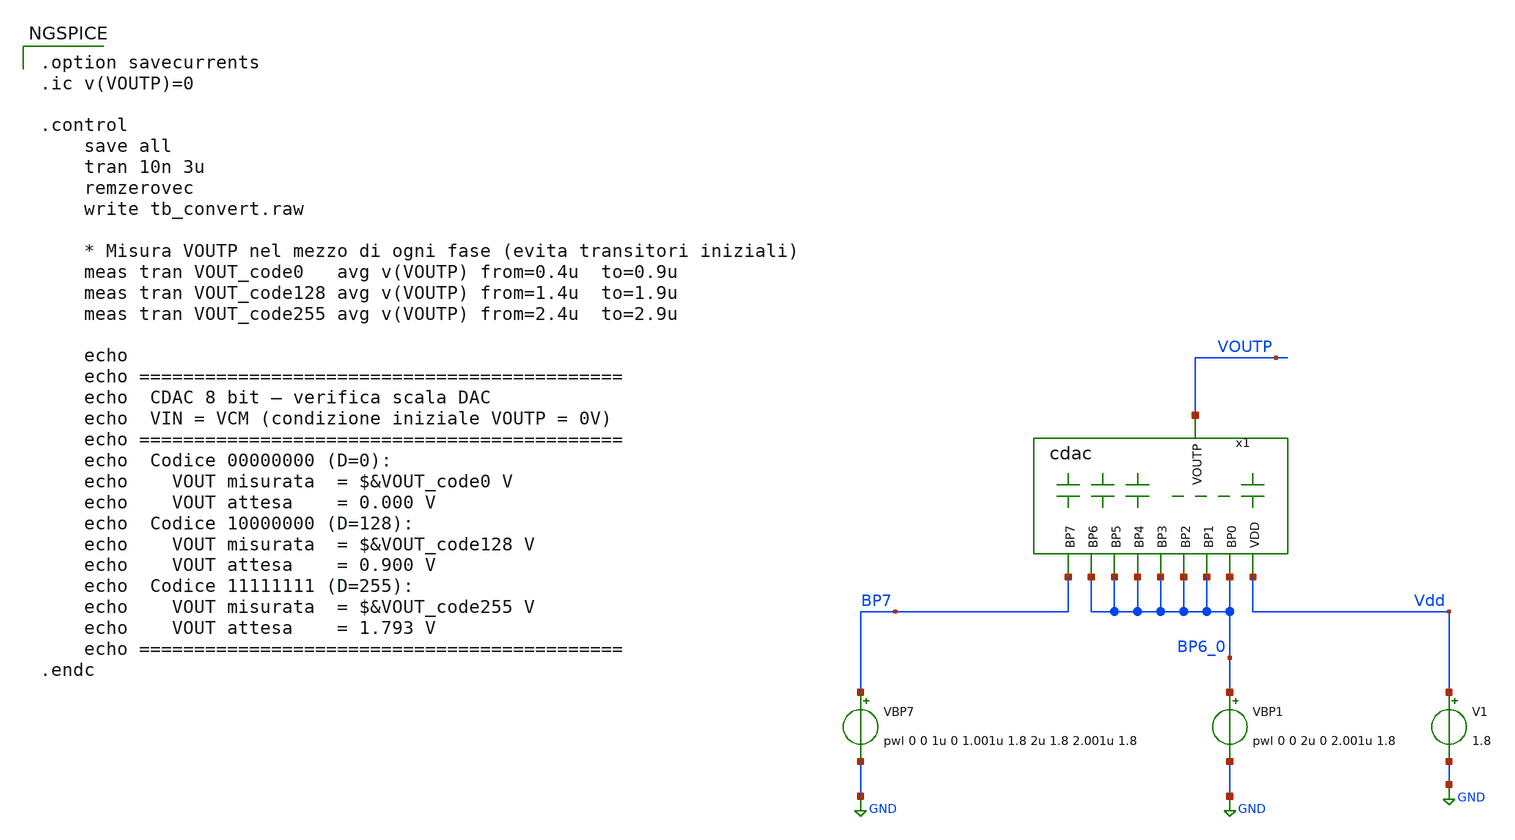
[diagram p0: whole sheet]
** sch_path: 02_sky130_pdk/soluzioni/lab_cdac/xschem/tb_convert.sch
**.subckt tb_convert
VBP7 BP7 GND pwl 0 0 1u 0 1.001u 1.8 2u 1.8 2.001u 1.8
VBP1 BP6_0 GND pwl 0 0 2u 0 2.001u 1.8
x1 VOUTP Vdd BP6_0 BP6_0 BP6_0 BP6_0 BP6_0 BP6_0 BP7 BP6_0 cdac
V1 Vdd GND 1.8
**** begin user architecture code

** opencircuitdesign pdks install
.lib $::SKYWATER_MODELS/sky130.lib.spice tt


.option savecurrents
.ic v(VOUTP)=0

.control
    save all
    tran 10n 3u
    remzerovec
    write tb_convert.raw

    * Misura VOUTP nel mezzo di ogni fase (evita transitori iniziali)
    meas tran VOUT_code0   avg v(VOUTP) from=0.4u  to=0.9u
    meas tran VOUT_code128 avg v(VOUTP) from=1.4u  to=1.9u
    meas tran VOUT_code255 avg v(VOUTP) from=2.4u  to=2.9u

    echo
    echo ============================================
    echo  CDAC 8 bit — verifica scala DAC
    echo  VIN = VCM (condizione iniziale VOUTP = 0V)
    echo ============================================
    echo  Codice 00000000 (D=0):
    echo    VOUT misurata  = $&VOUT_code0 V
    echo    VOUT attesa    = 0.000 V
    echo  Codice 10000000 (D=128):
    echo    VOUT misurata  = $&VOUT_code128 V
    echo    VOUT attesa    = 0.900 V
    echo  Codice 11111111 (D=255):
    echo    VOUT misurata  = $&VOUT_code255 V
    echo    VOUT attesa    = 1.793 V
    echo ============================================
.endc

**** end user architecture code
**.ends

* expanding   symbol:  cdac.sym # of pins=10
** sym_path: 02_sky130_pdk/soluzioni/lab_cdac/xschem/cdac.sym
** sch_path: 02_sky130_pdk/soluzioni/lab_cdac/xschem/cdac.sch
.subckt cdac VOUTP VDD BP3 BP2 BP5 BP4 BP1 BP6 BP7 BP0
*.ipin VDD
*.opin VOUTP
*.ipin BP0
*.ipin BP1
*.ipin BP2
*.ipin BP3
*.ipin BP4
*.ipin BP5
*.ipin BP6
*.ipin BP7
XC1 VDD VOUTP sky130_fd_pr__cap_mim_m3_1 W=5 L=5 MF=1 m=1
XC2 BP0 VOUTP sky130_fd_pr__cap_mim_m3_1 W=5 L=5 MF=1 m=1
XC3 BP1 VOUTP sky130_fd_pr__cap_mim_m3_1 W=5 L=5 MF=2 m=2
XC4 BP2 VOUTP sky130_fd_pr__cap_mim_m3_1 W=5 L=5 MF=4 m=4
XC5 BP3 VOUTP sky130_fd_pr__cap_mim_m3_1 W=5 L=5 MF=8 m=8
XC6 BP4 VOUTP sky130_fd_pr__cap_mim_m3_1 W=5 L=5 MF=16 m=16
XC7 BP5 VOUTP sky130_fd_pr__cap_mim_m3_1 W=5 L=5 MF=32 m=32
XC8 BP6 VOUTP sky130_fd_pr__cap_mim_m3_1 W=5 L=5 MF=64 m=64
XC9 BP7 VOUTP sky130_fd_pr__cap_mim_m3_1 W=5 L=5 MF=128 m=128
.ends

.GLOBAL GND
.end
